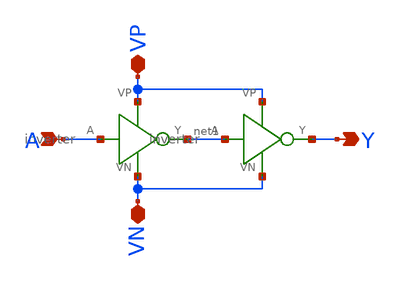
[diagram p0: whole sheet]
** sch_path: MP1/buffer.sch
**.subckt buffer A VP VN Y
*.ipin A
*.iopin VP
*.iopin VN
*.opin Y
**.ends

* expanding   symbol:  /home/madvlsi/Desktop/MP1/inverter.sym # of pins=4
** sym_path: MP1/inverter.sym
** sch_path: MP1/inverter.sch
.subckt inverter A Y VP VN
*.ipin A
*.iopin VP
*.iopin VN
*.iopin Y
XM1 Y A VN VN sky130_fd_pr__nfet_01v8 L=0.15 W=1 nf=1 ad='int((nf+1)/2) * W/nf * 0.29' as='int((nf+2)/2) * W/nf * 0.29'
+ pd='2*int((nf+1)/2) * (W/nf + 0.29)' ps='2*int((nf+2)/2) * (W/nf + 0.29)' nrd='0.29 / W' nrs='0.29 / W'
+ sa=0 sb=0 sd=0 mult=1 m=1
XM2 Y A VP VP sky130_fd_pr__pfet_01v8 L=0.15 W=1 nf=1 ad='int((nf+1)/2) * W/nf * 0.29' as='int((nf+2)/2) * W/nf * 0.29'
+ pd='2*int((nf+1)/2) * (W/nf + 0.29)' ps='2*int((nf+2)/2) * (W/nf + 0.29)' nrd='0.29 / W' nrs='0.29 / W'
+ sa=0 sb=0 sd=0 mult=1 m=1
.ends

.end
